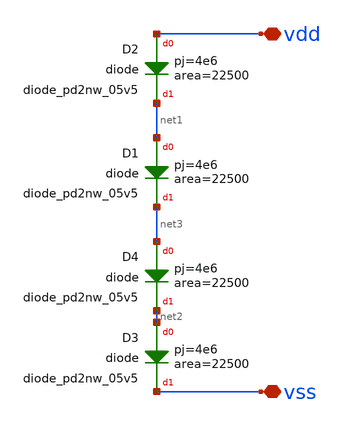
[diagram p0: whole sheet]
** sch_path: xschem/src/ESD/io_clamp.sch
**.subckt io_clamp vdd vss
*.iopin vdd
*.iopin vss
XD4 net3 net2 sky130_fd_pr__diode_pd2nw_05v5 area=22500 pj=4e6
XD1 net1 net3 sky130_fd_pr__diode_pd2nw_05v5 area=22500 pj=4e6
XD2 vdd net1 sky130_fd_pr__diode_pd2nw_05v5 area=22500 pj=4e6
XD3 net2 vss sky130_fd_pr__diode_pd2nw_05v5 area=22500 pj=4e6
**.ends
.end
